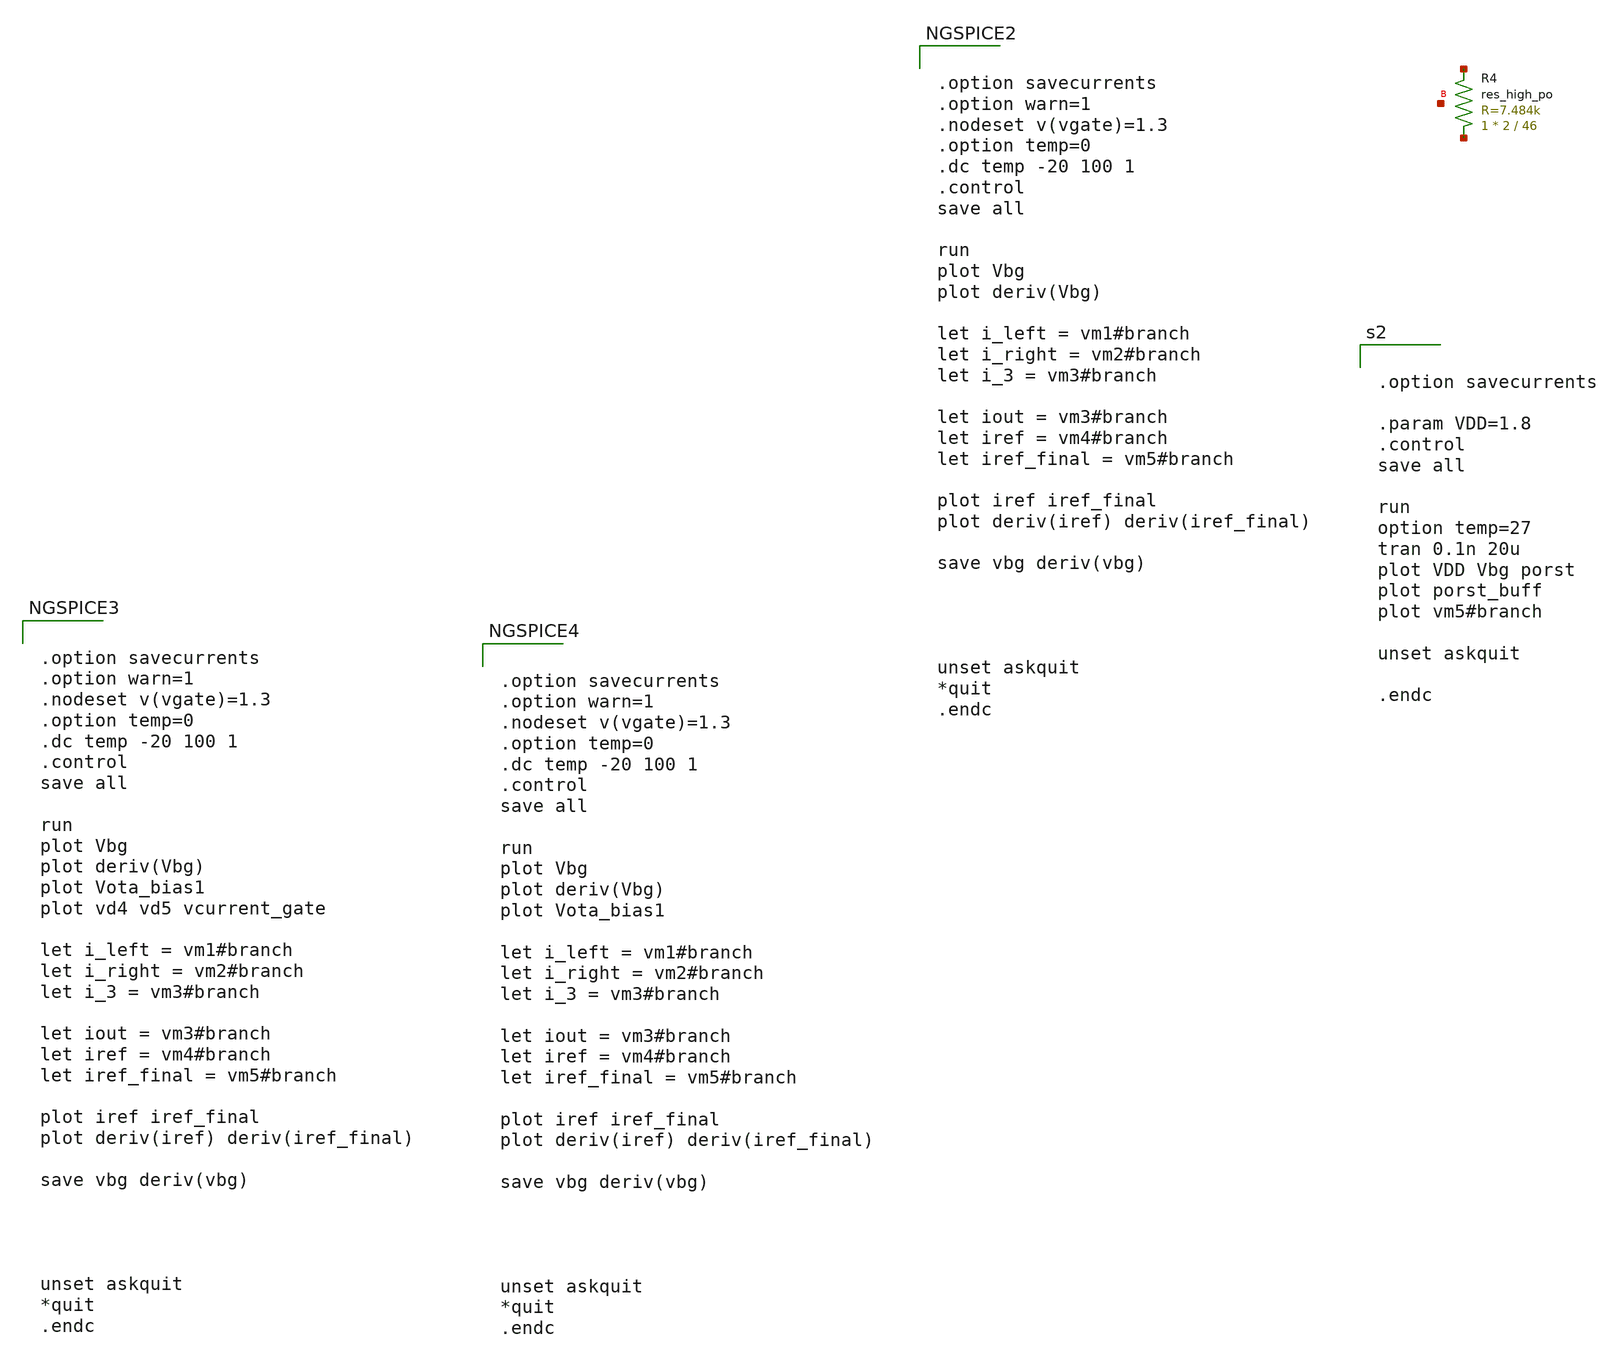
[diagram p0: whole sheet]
** sch_path: scratch.sch
**.subckt scratch
XR4 net1 net2 net3 sky130_fd_pr__res_high_po W=2 L=46 mult=1 m=1
**** begin user architecture code


.options savecurrents


.option
.control
save all
let startR = 20k
let endR = 30k
let incre = 1k
let curR = startR
while curR le endR
alter Rt curR
dc temp -40 100 1
write dc.out Vbg
set appendwrite
let curR = curR + incre
end
run

plot dc1.Vbg dc2.Vbg dc3.Vbg dc4.Vbg dc5.Vbg dc6.Vbg dc7.Vbg dc8.Vbg dc9.Vbg dc10.Vbg


.endc

*** plot voltage coefficient
*Vdd VDD GND 3.3
*V_en en GND 3.3
*.dc Vdd 2 4 0.1
*.control
*run
*plot deriv(V(Vbgp))
*.endc

*** plot temperature coefficient
*Vdd VDD GND 3.3
*V_en en GND 3.3
*.dc temp -40 140 1
*.control
*run
*plot deriv(V(Vbgp))/1.202344
*.endc



*** enable pin
*Vdd VDD GND 3.3
*V_en en GND PULSE(0 3.3 0 200us 200us 600us 2000us 0)
*.tran 1u 2000us
*.control
*run
*plot V(en)
*plot -I(VDD)
*.endc




.option savecurrents
.option warn=1
.param VDD=1.8
.param R3val='22.187k'
.param alpha='1'
.param R2R3ratio='5.6555038*alpha'
.param R2val='R3val*R2R3ratio'
.param R4R2ratio=0.79694273
.param R4val='R2val*R4R2ratio'
.nodeset v(vgate)=1.3
.option temp=0
.dc temp -40 100 1
.control
save all
*+ @m.xm13.msky130_fd_pr__pfet_01v8_lvt[gm]
*+ @m.xm3.msky130_fd_pr__pfet_01v8_lvt[gm]
*+ @m.xm4.msky130_fd_pr__pfet_01v8_lvt[gm]
*+ @m.xm5.msky130_fd_pr__nfet_01v8_lvt[gm]
*+ @m.xm6.msky130_fd_pr__nfet_01v8_lvt[gm]
*+ @m.xm7.msky130_fd_pr__nfet_01v8_lvt[gm]
*+ @m.xm8.msky130_fd_pr__pfet_01v8_lvt[gm]
*+ @m.xm9.msky130_fd_pr__nfet_01v8_lvt[gm]
run
plot Vbg
plot deriv(Vbg)
plot vota_bias
let i_bias = vmbias#branch
plot i_bias
*plot vbg vfeedback vcurrent_gate
let i_left = vm1#branch
let i_right = vm2#branch
let i_3 = vm3#branch
plot i_left i_right i_3
plot i_3
plot deriv(i_3)
plot va vb vbe3 vgate
plot Veb vbneg
plot vbe3
plot deriv(vbe3)
let iout = vm3#branch
let iref = vm4#branch
let iref_final = vm5#branch
*plot iout iref iref_final
*plot iref iref_final
*plot deriv(iout) deriv(iref) deriv(iref_final)
*plot vcurrent_gate vd5 vd4
save vbg deriv(vbg)


let indx27 = 3700
let indx0 = 1000
let indx70 = 8000
*indx is the index of temperature sweep for 27degC
echo 'Vbg @ 27degC'
let vbg27c = vbg[indx27]
print vbg27c
echo 'dVbe/degC & ppm @ 27degC'
print deriv(vbg)[indx27] deriv(vbg)[indx27]/vbg27c
echo 'ppm real'
print (vbg[indx70]-vbg[indx0])/vbg[indx27]/(70-0)*1e6
*plot deriv(vbg)/vbg27c
*plot v(va, vb) vs i
*plot vm1#branch vm2#branch vm3#branch
save deriv(vbg)/vbg27c
let vsg = vdd - vgate
let vsd1 = vdd - va
let vsd2 = vdd - vb
let vsd3 = vdd - vbg
*let vthp = @m.xm1.msky130_fd_pr__pfet_01v8_lvt['vth']
*let vov = vsg - vthp
**plot vov vsd1 vsd2 vsd3
*let deltav = vb - vbneg
*let r4 =vbg/vm3#branch
*let r1 =va/vr1#branch
*let r2 =vb/vr4#branch
*let r3 =deltav/vr2#branch
*let vptat =(r2/r3*deltav)
*let sum = veb+vptat
**plot veb vptat sum
**plot deriv(veb) deriv(vptat)
*save veb vptat sum deriv(veb) deriv(vptat)
*let gm1=@m.xm1.msky130_fd_pr__pfet_01v8_lvt[gm]
*let gm2=@m.xm2.msky130_fd_pr__pfet_01v8_lvt[gm]
*let Av2=gm2 * ((r3 + r3/ln(39)) * r2 / (r3 + r3/ln(39) + r2) )
*let Av1=gm1 * (r1 * r3/ln(39))/(r1 + r3/ln(39))
**plot Av1 Av2 Av2/Av1
*let gm13=@m.xm13.msky130_fd_pr__pfet_01v8_lvt[gm]
*let gm3=@m.xm3.msky130_fd_pr__pfet_01v8_lvt[gm]
*let gm4=@m.xm4.msky130_fd_pr__pfet_01v8_lvt[gm]
*let gm5=@m.xm5.msky130_fd_pr__nfet_01v8_lvt[gm]
*let gm6=@m.xm6.msky130_fd_pr__nfet_01v8_lvt[gm]
*let gm7=@m.xm7.msky130_fd_pr__nfet_01v8_lvt[gm]
*let gm8=@m.xm8.msky130_fd_pr__pfet_01v8_lvt[gm]
*let gm9=@m.xm9.msky130_fd_pr__nfet_01v8_lvt[gm]
*let vdsat1=2/(gm1/vm1#branch)
*let vdsat2=2/(gm2/vm2#branch)
*let vdsat3=2/(gm3/vm3#branch)
*let vdsat4=2/(gm4/@m.xm4.msky130_fd_pr__pfet_01v8_lvt[id])
*let vdsat5=2/(gm5/@m.xm5.msky130_fd_pr__nfet_01v8_lvt[id])
*let vdsat6=2/(gm6/@m.xm6.msky130_fd_pr__nfet_01v8_lvt[id])
*let vdsat7=2/(gm7/@m.xm7.msky130_fd_pr__nfet_01v8_lvt[id])
*let vdsat8=2/(gm8/@m.xm8.msky130_fd_pr__pfet_01v8_lvt[id])
*let vdsat9=2/(gm9/@m.xm9.msky130_fd_pr__nfet_01v8_lvt[id])
*let vdsat13=2/(gm13/@m.xm13.msky130_fd_pr__pfet_01v8_lvt[id])
*save (vdd-va-vdsat1) (vdd-vb-vdsat2) (vdd-vbg-vdsat3)
*+ (vdd-vgate-vdsat4) (vgate-vq-vdsat5) (vq-0-vdsat6)
*+ (vx-0-vdsat7) (vdd-vg-vdsat8) (vg-vq-vdsat9) (vdd-vx-vdsat13)

unset askquit
*quit
.endc




.options savecurrents

*** plot temperature coefficient
*Vdd VDD GND 3.3
*V_en en GND 3.3
*.dc temp -40 140 1
.control
*run
*dc temp -40 100 1
*plot Vout

save all
set appendwrite
compose width_vector  values 1.25 2
compose length_vector values 0.15 1

let i = 0
while i < length(width_vector)
    reset
    echo 'assigning vectors'
    alter @m.xm1.msky130_fd_pr__nfet_01v8[L] = length_vector[i]
    echo 'Still assigning vectors'
    alter @m.xm1.msky130_fd_pr__nfet_01v8[W] = width_vector[i]
    echo 'done assigning'
    dc temp -40 100 1
    plot Vout

    let i = i + 1
end


.endc



*** plot voltage coefficient
*Vdd VDD GND 3.3
*V_en en GND 3.3
*.dc Vdd 2 4 0.1
*.control
*run
*plot deriv(V(Vbgp))
*.endc

*** plot temperature coefficient
*Vdd VDD GND 3.3
*V_en en GND 3.3
*.dc temp -40 140 1
*.control
*run
*plot deriv(V(Vbgp))/1.202344
*.endc



*** enable pin
*Vdd VDD GND 3.3
*V_en en GND PULSE(0 3.3 0 200us 200us 600us 2000us 0)
*.tran 1u 2000us
*.control
*run
*plot V(en)
*plot -I(VDD)
*.endc




.options savecurrents

*** plot temperature coefficient
*Vdd VDD GND 3.3
*V_en en GND 3.3
*.dc temp -40 140 1
.control
save all
run
dc temp -40 100 1
plot Vbg




.endc



*** plot voltage coefficient
*Vdd VDD GND 3.3
*V_en en GND 3.3
*.dc Vdd 2 4 0.1
*.control
*run
*plot deriv(V(Vbgp))
*.endc

*** plot temperature coefficient
*Vdd VDD GND 3.3
*V_en en GND 3.3
*.dc temp -40 140 1
*.control
*run
*plot deriv(V(Vbgp))/1.202344
*.endc



*** enable pin
*Vdd VDD GND 3.3
*V_en en GND PULSE(0 3.3 0 200us 200us 600us 2000us 0)
*.tran 1u 2000us
*.control
*run
*plot V(en)
*plot -I(VDD)
*.endc




.option savecurrents
.option warn=1
.nodeset v(vgate)=1.3
.option temp=0
.dc temp -20 100 1
.control
save all

run
plot Vbg
plot deriv(Vbg)

let i_left = vm1#branch
let i_right = vm2#branch
let i_3 = vm3#branch

let iout = vm3#branch
let iref = vm4#branch
let iref_final = vm5#branch

plot iref iref_final
plot deriv(iref) deriv(iref_final)

save vbg deriv(vbg)




unset askquit
*quit
.endc




.option savecurrents
.option warn=1
.nodeset v(vgate)=1.3
.option temp=0
.dc temp -20 100 1
.control
save all

run
plot Vbg
plot deriv(Vbg)
plot Vota_bias1

let i_left = vm1#branch
let i_right = vm2#branch
let i_3 = vm3#branch

let iout = vm3#branch
let iref = vm4#branch
let iref_final = vm5#branch

plot iref iref_final
plot deriv(iref) deriv(iref_final)

save vbg deriv(vbg)




unset askquit
*quit
.endc




.option savecurrents
.option warn=1
.nodeset v(vgate)=1.3
.option temp=0
.dc temp -20 100 1
.control
save all

run
plot Vbg
plot deriv(Vbg)
plot Vota_bias1
plot vd4 vd5 vcurrent_gate

let i_left = vm1#branch
let i_right = vm2#branch
let i_3 = vm3#branch

let iout = vm3#branch
let iref = vm4#branch
let iref_final = vm5#branch

plot iref iref_final
plot deriv(iref) deriv(iref_final)

save vbg deriv(vbg)




unset askquit
*quit
.endc




.option savecurrents

.param VDD=1.8
.control
save all

run
option temp=27
tran 0.1n 20u
plot VDD Vbg porst
plot porst_buff
plot vm5#branch

unset askquit

.endc


**** end user architecture code
**.ends
.end
